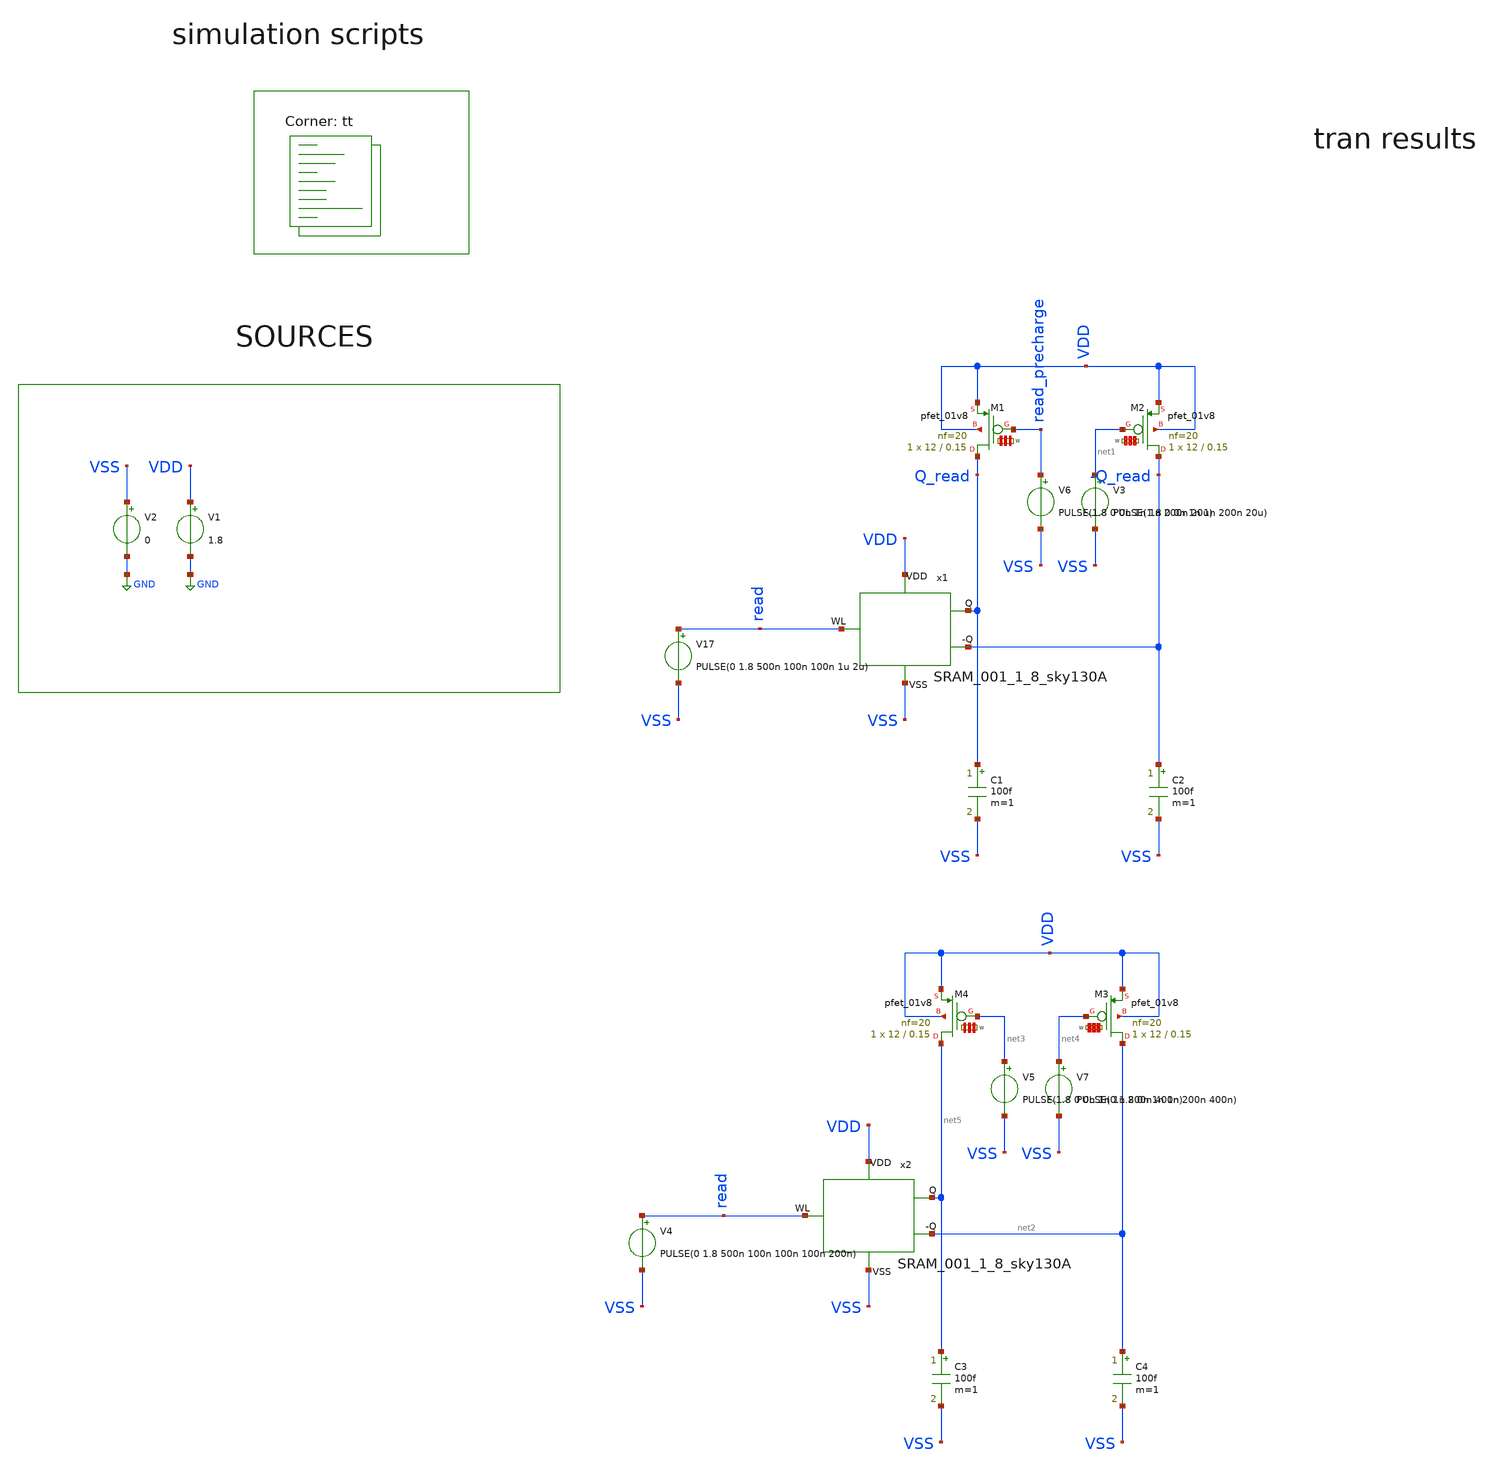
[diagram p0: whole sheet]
** sch_path: my_ip/sky130A/Memory_tb/tb.sch
**.subckt tb
V1 VDD GND 1.8
V2 VSS GND 0
V17 read VSS PULSE(0 1.8 500n 100n 100n 1u 2u)
x1 VDD VSS read Q_read -Q_read SRAM_001_1_8_sky130A
C1 Q_read VSS 100f m=1
V6 read_precharge VSS PULSE(1.8 0 0n 1n 1n 200n 20u)
XM2 -Q_read net1 VDD VDD sky130_fd_pr__pfet_01v8 L=0.15 W='12 * 20 ' nf=20 ad= as='int((20 + 2)/2) * 12 * 0.29'
+ pd='2*int((20 + 1)/2) * (12 + 0.29)' ps='2*int((20 + 2)/2) * (12 + 0.29)' nrd='0.29 / 12 / 20 ' nrs='0.29 / 12 / 20 '
+ sa=0 sb=0 sd=0 mult=1 m=1
XM1 Q_read read_precharge VDD VDD sky130_fd_pr__pfet_01v8 L=0.15 W='12 * 20 ' nf=20 ad= as='int((20 + 2)/2) * 12 * 0.29'
+ pd='2*int((20 + 1)/2) * (12 + 0.29)' ps='2*int((20 + 2)/2) * (12 + 0.29)' nrd='0.29 / 12 / 20 ' nrs='0.29 / 12 / 20 '
+ sa=0 sb=0 sd=0 mult=1 m=1
V3 net1 VSS PULSE(1.8 0 0n 1n 1n 200n 20u)
C2 -Q_read VSS 100f m=1
V4 read VSS PULSE(0 1.8 500n 100n 100n 100n 200n)
x2 VDD VSS read net5 net2 SRAM_001_1_8_sky130A
C3 net5 VSS 100f m=1
V5 net3 VSS PULSE(1.8 0 0n 1n 1n 200n 400n)
XM3 net2 net4 VDD VDD sky130_fd_pr__pfet_01v8 L=0.15 W='12 * 20 ' nf=20 ad= as='int((20 + 2)/2) * 12 * 0.29'
+ pd='2*int((20 + 1)/2) * (12 + 0.29)' ps='2*int((20 + 2)/2) * (12 + 0.29)' nrd='0.29 / 12 / 20 ' nrs='0.29 / 12 / 20 '
+ sa=0 sb=0 sd=0 mult=1 m=1
XM4 net5 net3 VDD VDD sky130_fd_pr__pfet_01v8 L=0.15 W='12 * 20 ' nf=20 ad= as='int((20 + 2)/2) * 12 * 0.29'
+ pd='2*int((20 + 1)/2) * (12 + 0.29)' ps='2*int((20 + 2)/2) * (12 + 0.29)' nrd='0.29 / 12 / 20 ' nrs='0.29 / 12 / 20 '
+ sa=0 sb=0 sd=0 mult=1 m=1
V7 net4 VSS PULSE(0 1.8 0n 1n 1n 200n 400n)
C4 net2 VSS 100f m=1
**** begin user architecture code
.lib $::SKYWATER_MODELS/sky130.lib.spice tt

**************************************************************
**************************************************************
**************************************************************
**************************************************************
**************************************************************
*LIBs*********************************************************
**************************************************************
**************************************************************
**************************************************************
**************************************************************
**************************************************************
*.lib $::SKYWATER_MODELS/sky130.lib.spice tt
* chose the corners in the corner file
* tt_mm for mismatch
* ss ff sf fs standart corners
* ll hh lh hl capacitor and resistors corners
* mc for total process variation including corners
**************************************************************
**************************************************************
**************************************************************
**************************************************************
**************************************************************
*Corners/montecarlo options***********************************
**************************************************************
**************************************************************
**************************************************************
**************************************************************
**************************************************************
.TEMP 27
**************************************************************
**************************************************************
**************************************************************
**************************************************************
*SIMULATION and Plots*****************************************
**************************************************************
**************************************************************
**************************************************************
**************************************************************
.control
save all
save @m.x1.xm1.msky130_fd_pr__pfet_01v8[gm]
save @m.x1.xm1.msky130_fd_pr__pfet_01v8[vth]
save @m.x1.xm1.msky130_fd_pr__pfet_01v8[gds]
save @m.x1.xm1.msky130_fd_pr__pfet_01v8[gmbs]
save @m.x1.xm1.msky130_fd_pr__pfet_01v8[vds]
save @m.x1.xm1.msky130_fd_pr__pfet_01v8[vgs]


save @m.x1.xm2.msky130_fd_pr__pfet_01v8_lvt[gm]
save @m.x1.xm2.msky130_fd_pr__pfet_01v8_lvt[vth]
save @m.x1.xm2.msky130_fd_pr__pfet_01v8_lvt[gds]
save @m.x1.xm2.msky130_fd_pr__pfet_01v8_lvt[gmbs]
save @m.x1.xm2.msky130_fd_pr__pfet_01v8_lvt[vds]
save @m.x1.xm2.msky130_fd_pr__pfet_01v8_lvt[vgs]

save @m.x1.xm3.msky130_fd_pr__nfet_01v8[gm]
save @m.x1.xm3.msky130_fd_pr__nfet_01v8[vth]
save @m.x1.xm3.msky130_fd_pr__nfet_01v8[gds]
save @m.x1.xm3.msky130_fd_pr__nfet_01v8[gmbs]
save @m.x1.xm3.msky130_fd_pr__nfet_01v8[vds]
save @m.x1.xm3.msky130_fd_pr__nfet_01v8[vgs]

save @m.x1.xm4.msky130_fd_pr__nfet_01v8[gm]
save @m.x1.xm4.msky130_fd_pr__nfet_01v8[vth]
save @m.x1.xm4.msky130_fd_pr__nfet_01v8[gds]
save @m.x1.xm4.msky130_fd_pr__nfet_01v8[gmbs]
save @m.x1.xm4.msky130_fd_pr__nfet_01v8[vds]
save @m.x1.xm4.msky130_fd_pr__nfet_01v8[vgs]

save @m.x1.xm5.msky130_fd_pr__nfet_01v8[gm]
save @m.x1.xm5.msky130_fd_pr__nfet_01v8[vth]
save @m.x1.xm5.msky130_fd_pr__nfet_01v8[gds]
save @m.x1.xm5.msky130_fd_pr__nfet_01v8[gmbs]
save @m.x1.xm5.msky130_fd_pr__nfet_01v8[vds]
save @m.x1.xm5.msky130_fd_pr__nfet_01v8[vgs]

save @m.x1.xm6.msky130_fd_pr__nfet_01v8[gm]
save @m.x1.xm6.msky130_fd_pr__nfet_01v8[vth]
save @m.x1.xm6.msky130_fd_pr__nfet_01v8[gds]
save @m.x1.xm6.msky130_fd_pr__nfet_01v8[gmbs]
save @m.x1.xm6.msky130_fd_pr__nfet_01v8[vds]
save @m.x1.xm6.msky130_fd_pr__nfet_01v8[vgs]

save @m.x1.xm7.msky130_fd_pr__pfet_01v8_lvt[gm]
save @m.x1.xm7.msky130_fd_pr__pfet_01v8_lvt[vth]
save @m.x1.xm7.msky130_fd_pr__pfet_01v8_lvt[gds]
save @m.x1.xm7.msky130_fd_pr__pfet_01v8_lvt[gmbs]
save @m.x1.xm7.msky130_fd_pr__pfet_01v8_lvt[vds]
save @m.x1.xm7.msky130_fd_pr__pfet_01v8_lvt[vgs]

save @m.x1.xm8.msky130_fd_pr__pfet_01v8_lvt[gm]
save @m.x1.xm8.msky130_fd_pr__pfet_01v8_lvt[vth]
save @m.x1.xm8.msky130_fd_pr__pfet_01v8_lvt[gds]
save @m.x1.xm8.msky130_fd_pr__pfet_01v8_lvt[gmbs]
save @m.x1.xm8.msky130_fd_pr__pfet_01v8_lvt[vds]
save @m.x1.xm8.msky130_fd_pr__pfet_01v8_lvt[vgs]

save @m.x1.xm9.msky130_fd_pr__pfet_01v8_lvt[gm]
save @m.x1.xm9.msky130_fd_pr__pfet_01v8_lvt[vth]
save @m.x1.xm9.msky130_fd_pr__pfet_01v8_lvt[gds]
save @m.x1.xm9.msky130_fd_pr__pfet_01v8_lvt[gmbs]
save @m.x1.xm9.msky130_fd_pr__pfet_01v8_lvt[vds]
save @m.x1.xm9.msky130_fd_pr__pfet_01v8_lvt[vgs]


save @m.x1.xm10.msky130_fd_pr__nfet_01v8[gm]
save @m.x1.xm10.msky130_fd_pr__nfet_01v8[vth]
save @m.x1.xm10.msky130_fd_pr__nfet_01v8[gds]
save @m.x1.xm10.msky130_fd_pr__nfet_01v8[gmbs]
save @m.x1.xm10.msky130_fd_pr__nfet_01v8[vds]
save @m.x1.xm10.msky130_fd_pr__nfet_01v8[vgs]


save @m.x1.xm11.msky130_fd_pr__nfet_01v8[gm]
save @m.x1.xm11.msky130_fd_pr__nfet_01v8[vth]
save @m.x1.xm11.msky130_fd_pr__nfet_01v8[gds]
save @m.x1.xm11.msky130_fd_pr__nfet_01v8[gmbs]
save @m.x1.xm11.msky130_fd_pr__nfet_01v8[vds]
save @m.x1.xm11.msky130_fd_pr__nfet_01v8[vgs]

save @m.x1.xm12.msky130_fd_pr__pfet_01v8_lvt[gm]
save @m.x1.xm12.msky130_fd_pr__pfet_01v8_lvt[vth]
save @m.x1.xm12.msky130_fd_pr__pfet_01v8_lvt[gds]
save @m.x1.xm12.msky130_fd_pr__pfet_01v8_lvt[gmbs]
save @m.x1.xm12.msky130_fd_pr__pfet_01v8_lvt[vds]
save @m.x1.xm12.msky130_fd_pr__pfet_01v8_lvt[vgs]

save @m.x1.xm13.msky130_fd_pr__nfet_01v8[gm]
save @m.x1.xm13.msky130_fd_pr__nfet_01v8[vth]
save @m.x1.xm13.msky130_fd_pr__nfet_01v8[gds]
save @m.x1.xm13.msky130_fd_pr__nfet_01v8[gmbs]
save @m.x1.xm13.msky130_fd_pr__nfet_01v8[vds]
save @m.x1.xm13.msky130_fd_pr__nfet_01v8[vgs]

op
write tb.raw
set appendwrite


tran 100ps 5u
set appendwrite
write tb.raw

.endc

**** end user architecture code
**.ends

* expanding   symbol:  Memory/SRAM_001_1_8_sky130A.sym # of pins=5
** sym_path: my_ip/LIB/Memory/SRAM_001_1_8_sky130A.sym
** sch_path: my_ip/LIB/Memory/SRAM_001_1_8_sky130A.sch
.subckt SRAM_001_1_8_sky130A VDD VSS WL Q -Q
*.iopin VDD
*.iopin VSS
*.iopin WL
*.iopin Q
*.iopin -Q
XM1 a b VDD VDD sky130_fd_pr__pfet_01v8 L=0.15 W='2 * 6 ' nf=6 ad= as='int((6 + 2)/2) * 2 * 0.29' pd='2*int((6 + 1)/2) * (2 + 0.29)'
+ ps='2*int((6 + 2)/2) * (2 + 0.29)' nrd='0.29 / 2 / 6 ' nrs='0.29 / 2 / 6 ' sa=0 sb=0 sd=0 mult=2 m=2
XM2 a b VSS VSS sky130_fd_pr__nfet_01v8_lvt L=0.15 W='2 * 2 ' nf=2 ad='int((2 + 1)/2) * 2 / 2 * 0.29'
+ as='int((2 + 2)/2) * 2 / 2 * 0.29' pd='2*int((2 + 1)/2) * (2 / 2 + 0.29)' ps='2*int((2 + 2)/2) * (2 / 2 + 0.29)'
+ nrd='0.29 / 2 ' nrs='0.29 / 2 ' sa=0 sb=0 sd=0 mult=2 m=2
XM3 b a VSS VSS sky130_fd_pr__nfet_01v8_lvt L=0.15 W='2 * 2 ' nf=2 ad='int((2 + 1)/2) * 2 / 2 * 0.29'
+ as='int((2 + 2)/2) * 2 / 2 * 0.29' pd='2*int((2 + 1)/2) * (2 / 2 + 0.29)' ps='2*int((2 + 2)/2) * (2 / 2 + 0.29)'
+ nrd='0.29 / 2 ' nrs='0.29 / 2 ' sa=0 sb=0 sd=0 mult=2 m=2
XM4 b a VDD VDD sky130_fd_pr__pfet_01v8 L=0.15 W='2 * 6 ' nf=6 ad= as='int((6 + 2)/2) * 2 * 0.29' pd='2*int((6 + 1)/2) * (2 + 0.29)'
+ ps='2*int((6 + 2)/2) * (2 + 0.29)' nrd='0.29 / 2 / 6 ' nrs='0.29 / 2 / 6 ' sa=0 sb=0 sd=0 mult=2 m=2
XM5 Q WL a VSS sky130_fd_pr__nfet_01v8_lvt L=0.15 W='1 * 2 ' nf=2 ad='int((2 + 1)/2) * 1 / 2 * 0.29'
+ as='int((2 + 2)/2) * 1 / 2 * 0.29' pd='2*int((2 + 1)/2) * (1 / 2 + 0.29)' ps='2*int((2 + 2)/2) * (1 / 2 + 0.29)'
+ nrd='0.29 / 1 ' nrs='0.29 / 1 ' sa=0 sb=0 sd=0 mult=1 m=1
XM6 -Q WL b VSS sky130_fd_pr__nfet_01v8_lvt L=0.15 W='1 * 2 ' nf=2 ad='int((2 + 1)/2) * 1 / 2 * 0.29'
+ as='int((2 + 2)/2) * 1 / 2 * 0.29' pd='2*int((2 + 1)/2) * (1 / 2 + 0.29)' ps='2*int((2 + 2)/2) * (1 / 2 + 0.29)'
+ nrd='0.29 / 1 ' nrs='0.29 / 1 ' sa=0 sb=0 sd=0 mult=1 m=1
.ends

.GLOBAL GND
.end
